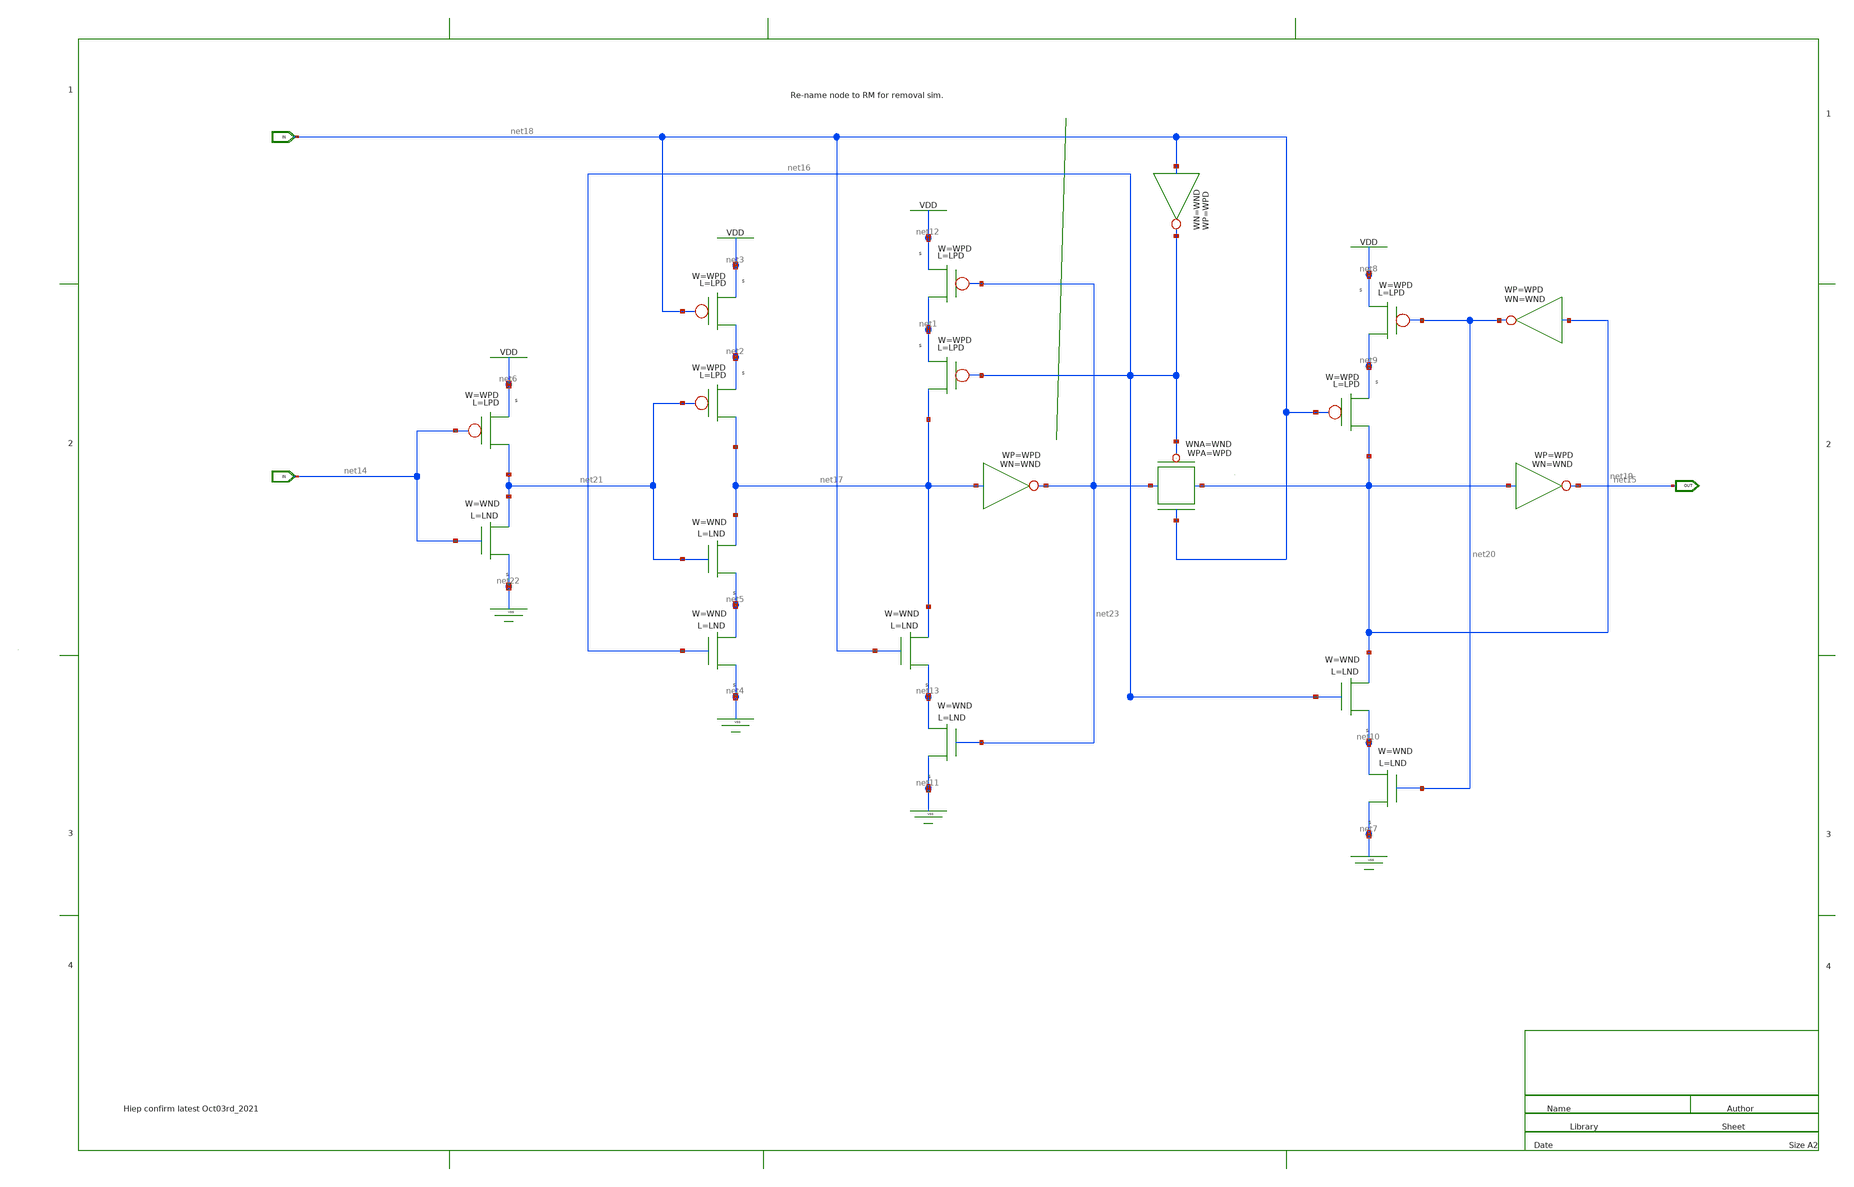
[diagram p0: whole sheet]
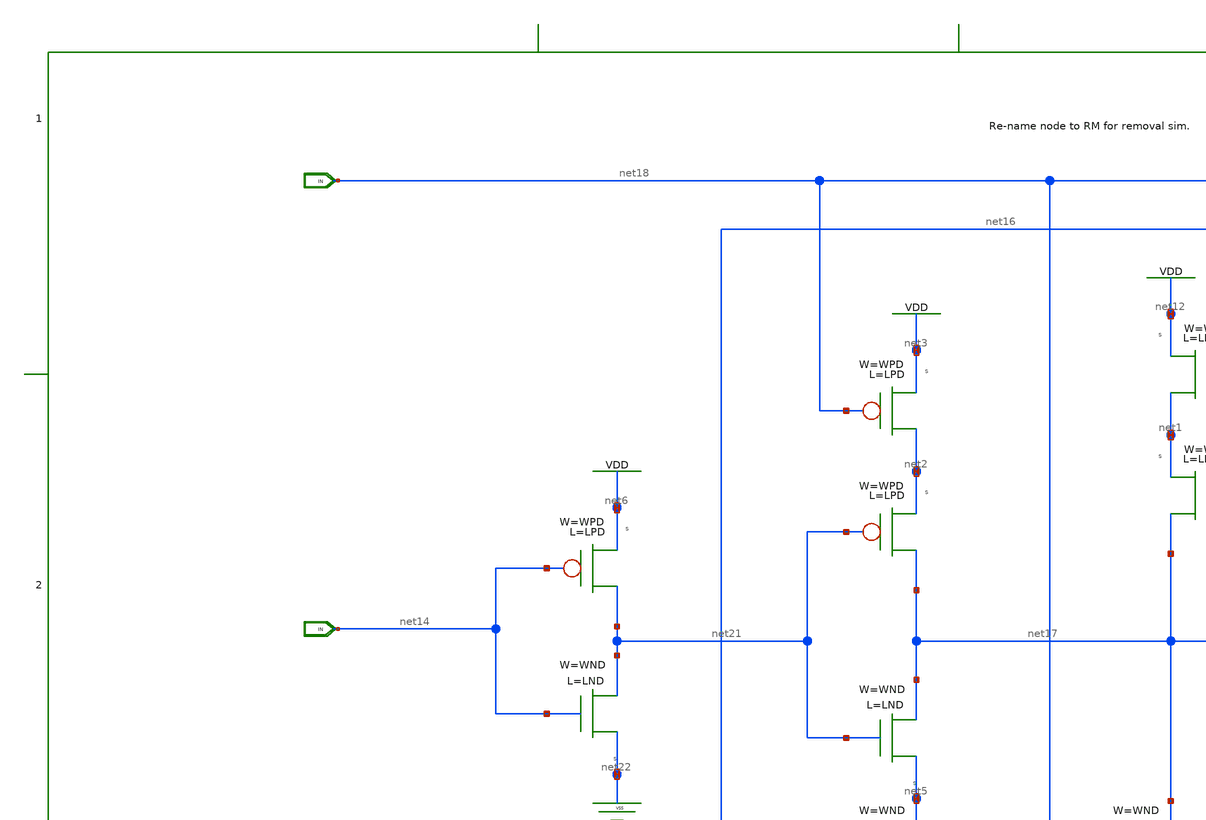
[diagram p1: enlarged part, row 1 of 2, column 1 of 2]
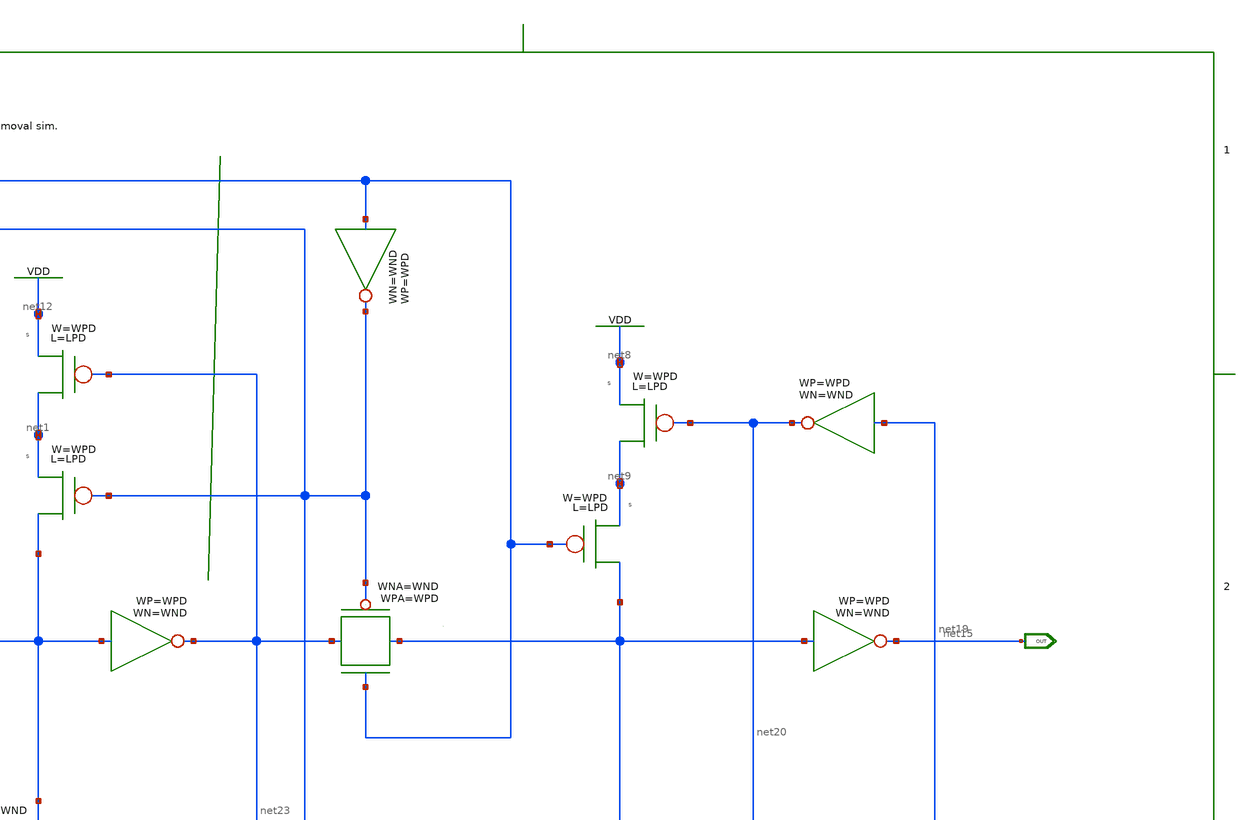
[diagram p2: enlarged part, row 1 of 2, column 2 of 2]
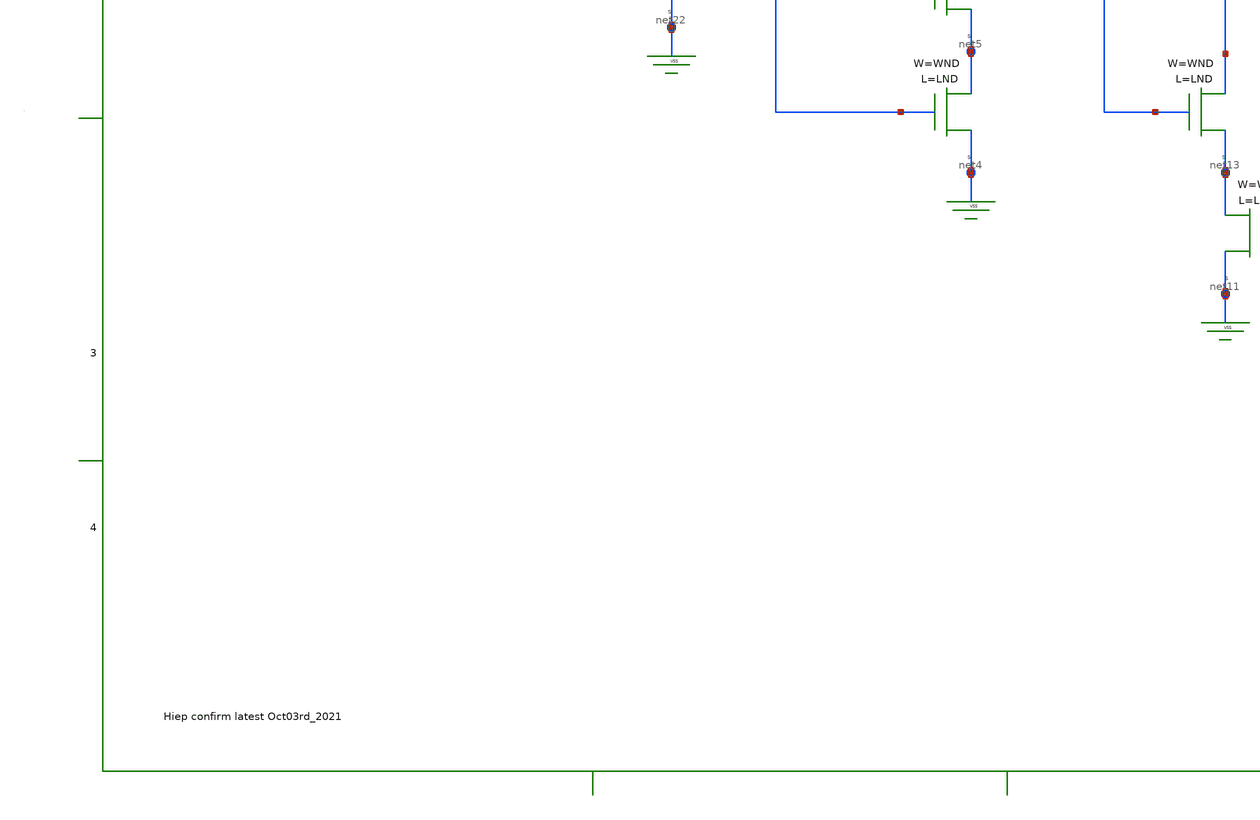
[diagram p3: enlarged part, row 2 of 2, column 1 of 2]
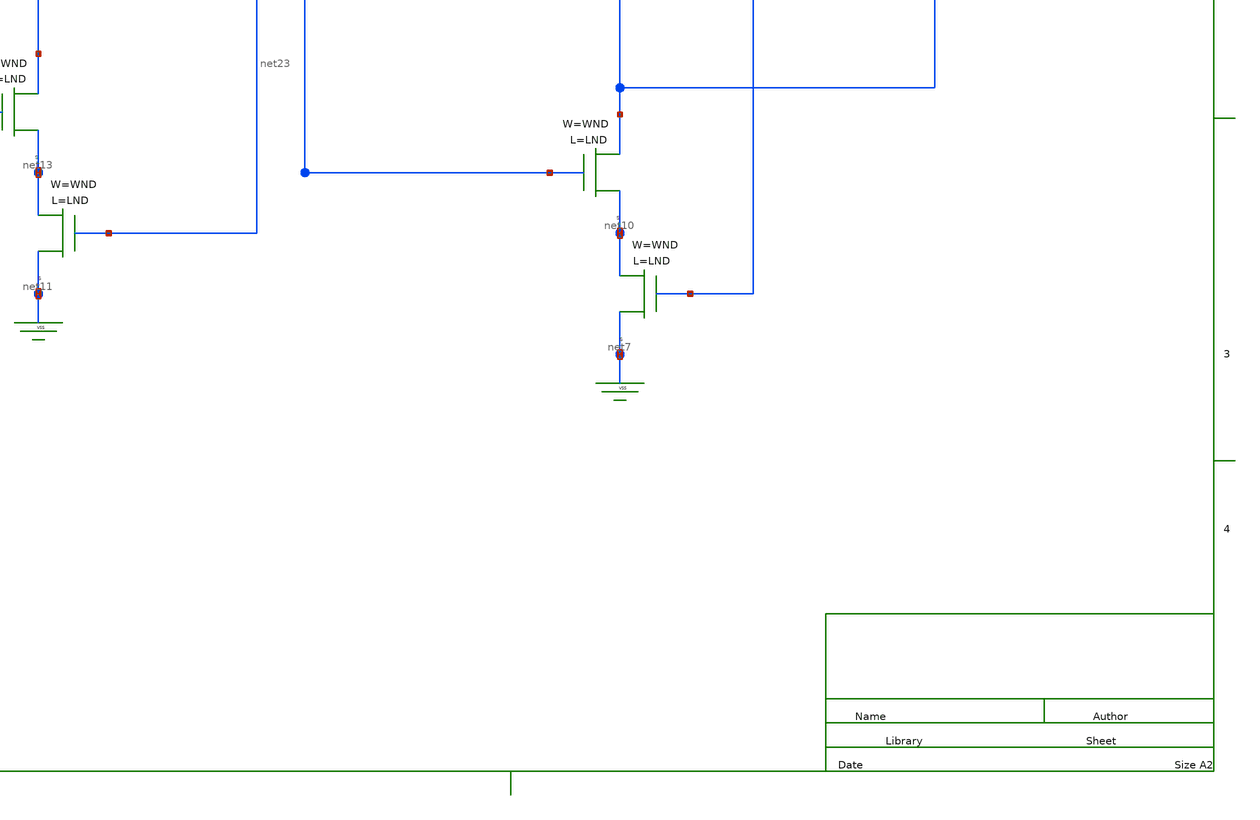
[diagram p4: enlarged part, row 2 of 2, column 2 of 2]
** sch_path: xschem_library/viewdraw_import/xschem_lib/dti_28hc_6p5t_40_ffqx1.sch
**.subckt dti_28hc_6p5t_40_ffqx1
**.ends
.end
